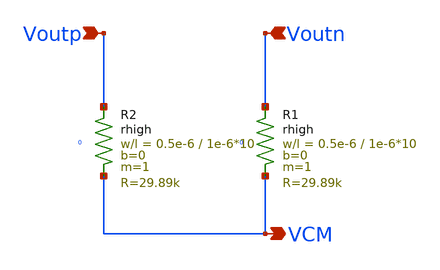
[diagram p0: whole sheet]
** sch_path: schema/ota_cmfb_cm_sense/ota_cmfb_cm_sense.sch
**.subckt ota_cmfb_cm_sense Voutp Voutn VCM
*.ipin Voutp
*.ipin Voutn
*.opin VCM
XR1 Voutn VCM 0 rhigh w=0.5e-6 l=1e-6*10 m=1 b=0 mm_ok=1
XR2 Voutp VCM 0 rhigh w=0.5e-6 l=1e-6*10 m=1 b=0 mm_ok=1
**.ends
.end
